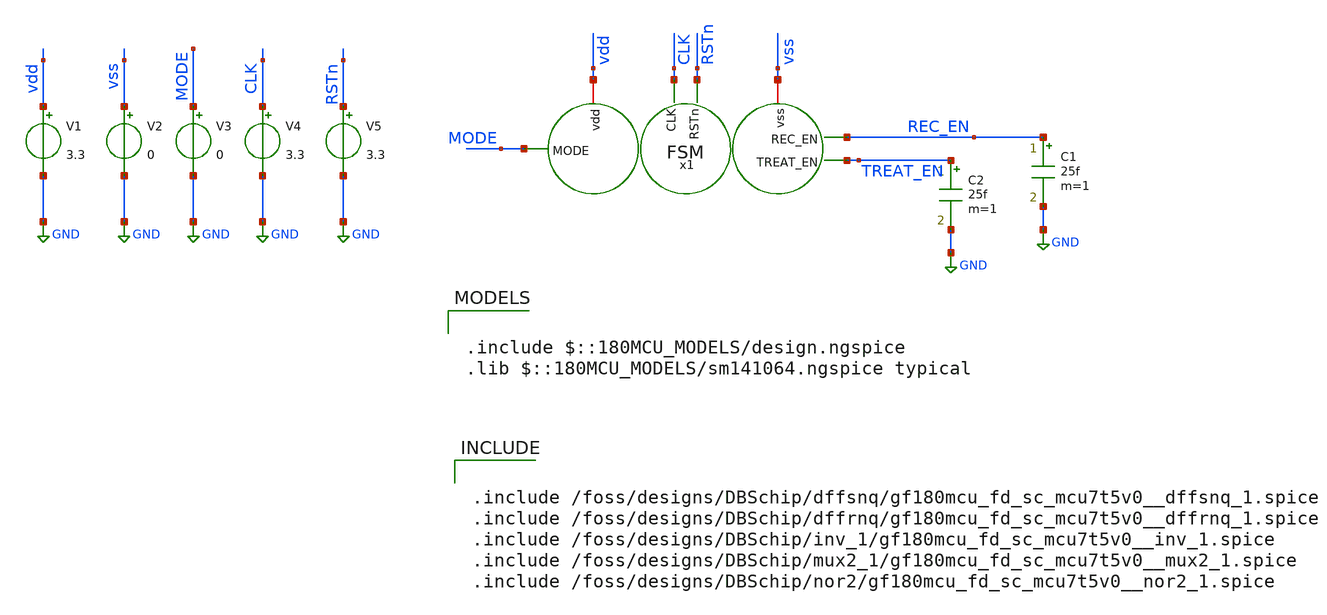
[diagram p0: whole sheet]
** sch_path: FSM_tb.sch
**.subckt FSM_tb
x1 REC_EN TREAT_EN MODE RSTn CLK vdd vss FSM
V1 vdd GND 3.3
V2 vss GND 0
V3 MODE GND 0
V4 CLK GND 3.3
V5 RSTn GND 3.3
C1 REC_EN GND 25f m=1
C2 TREAT_EN GND 25f m=1
**** begin user architecture code

.include $::180MCU_MODELS/design.ngspice
.lib $::180MCU_MODELS/sm141064.ngspice typical



.include /foss/designs/DBSchip/dffsnq/gf180mcu_fd_sc_mcu7t5v0__dffsnq_1.spice
.include /foss/designs/DBSchip/dffrnq/gf180mcu_fd_sc_mcu7t5v0__dffrnq_1.spice
.include /foss/designs/DBSchip/inv_1/gf180mcu_fd_sc_mcu7t5v0__inv_1.spice
.include /foss/designs/DBSchip/mux2_1/gf180mcu_fd_sc_mcu7t5v0__mux2_1.spice
.include /foss/designs/DBSchip/nor2/gf180mcu_fd_sc_mcu7t5v0__nor2_1.spice




.control
save all

** Define input signals
let fsig = 1e3
let tper = 1/fsig
let tper2 = 0.95*tper
let tfr = 0.01*tper
let ton_clk = 0.5*tper - 2*tfr

** Define transient params
let tstop  = 2*tper
let tstep  = 0.001 * tper
let tstop3 = 8*tstop

** --- D waveform: high in 1st+3rd quarters, low in 2nd+4th ---
** Achieve this by making D a square wave whose PERIOD = tstop3/2
** Then it is high for tstop3/4, low for tstop3/4, repeating.
let tper_D = tstop3/2
let ton_D  = 0.5*tper_D - 2*tfr

** --- async reset waveform: high first half, low second half ---
** Make one high pulse that lasts tstop3/2, with a very long period so it doesn't repeat.
let tper_R = 2*tstop3
let ton_R  = 0.5*tstop3 - 2*tfr

** NEW: fast clock independent of fsig
let fclk     = 1e5
let tper_clk = 1/fclk
let tper2clk = 0.95*tper_clk
let tfr_clk  = 0.01*tper_clk
let ton_clk  = 0.5*tper_clk - 2*tfr_clk

** Clock on V4 (unchanged)
alter @v4[PULSE] = [ 0 3.3 0 $&tfr_clk $&tfr_clk $&ton_clk $&tper2clk 0 ]

** D on V3 (quarter pattern across full tstop3)
alter @v3[PULSE] = [ 0 3.3 0 $&tfr $&tfr $&ton_D  $&tper_D 0 ]

** Async reset on V5 (high first half, low second half)
alter @v5[PULSE] = [ 0 3.3 0 $&tfr $&tfr $&ton_R  $&tper_R 0 ]

** Simulation
op
tran $&tstep $&tstop3

plot v(clk) v(mode)+5 v(rstn)+10 v(rec_en)+15 v(treat_en)+20

** Save waveform
write dff_tb.raw
.endc





**** end user architecture code
**.ends

* expanding   symbol:  FSM.sym # of pins=7
** sym_path: FSM/FSM.sym
** sch_path: FSM/FSM.sch
.subckt FSM REC_EN TREAT_EN MODE RSTn CLK vdd vss
*.opin REC_EN
*.ipin MODE
*.ipin RSTn
*.ipin CLK
*.opin TREAT_EN
*.iopin vdd
*.iopin vss
x1 REC_EN S0 TREAT_EN vdd vdd vss vss gf180mcu_fd_sc_mcu7t5v0__nor2_1
x2 TREAT_EN net1 net3 vdd vdd vss vss gf180mcu_fd_sc_mcu7t5v0__nor2_1
x3 MODE net1 vdd vdd net4 vss gf180mcu_fd_sc_mcu7t5v0__inv_1
x4 REC_EN TREAT_EN MODE net2 vdd vdd vss vss gf180mcu_fd_sc_mcu7t5v0__mux2_1
x5 net3 RSTn CLK REC_EN vdd vdd vss vss gf180mcu_fd_sc_mcu7t5v0__dffrnq_1
x6 net2 RSTn CLK S0 vdd vdd vss vss gf180mcu_fd_sc_mcu7t5v0__dffsnq_1
**** begin user architecture code


.include /foss/designs/DBSchip/dffsnq/gf180mcu_fd_sc_mcu7t5v0__dffsnq_1.spice
.include /foss/designs/DBSchip/dffrnq/gf180mcu_fd_sc_mcu7t5v0__dffrnq_1.spice
.include /foss/designs/DBSchip/inv_1/gf180mcu_fd_sc_mcu7t5v0__inv_1.spice
.include /foss/designs/DBSchip/mux2_1/gf180mcu_fd_sc_mcu7t5v0__mux2_1.spice
.include /foss/designs/DBSchip/nor2/gf180mcu_fd_sc_mcu7t5v0__nor2_1.spice


**** end user architecture code
.ends

.GLOBAL GND
.end
